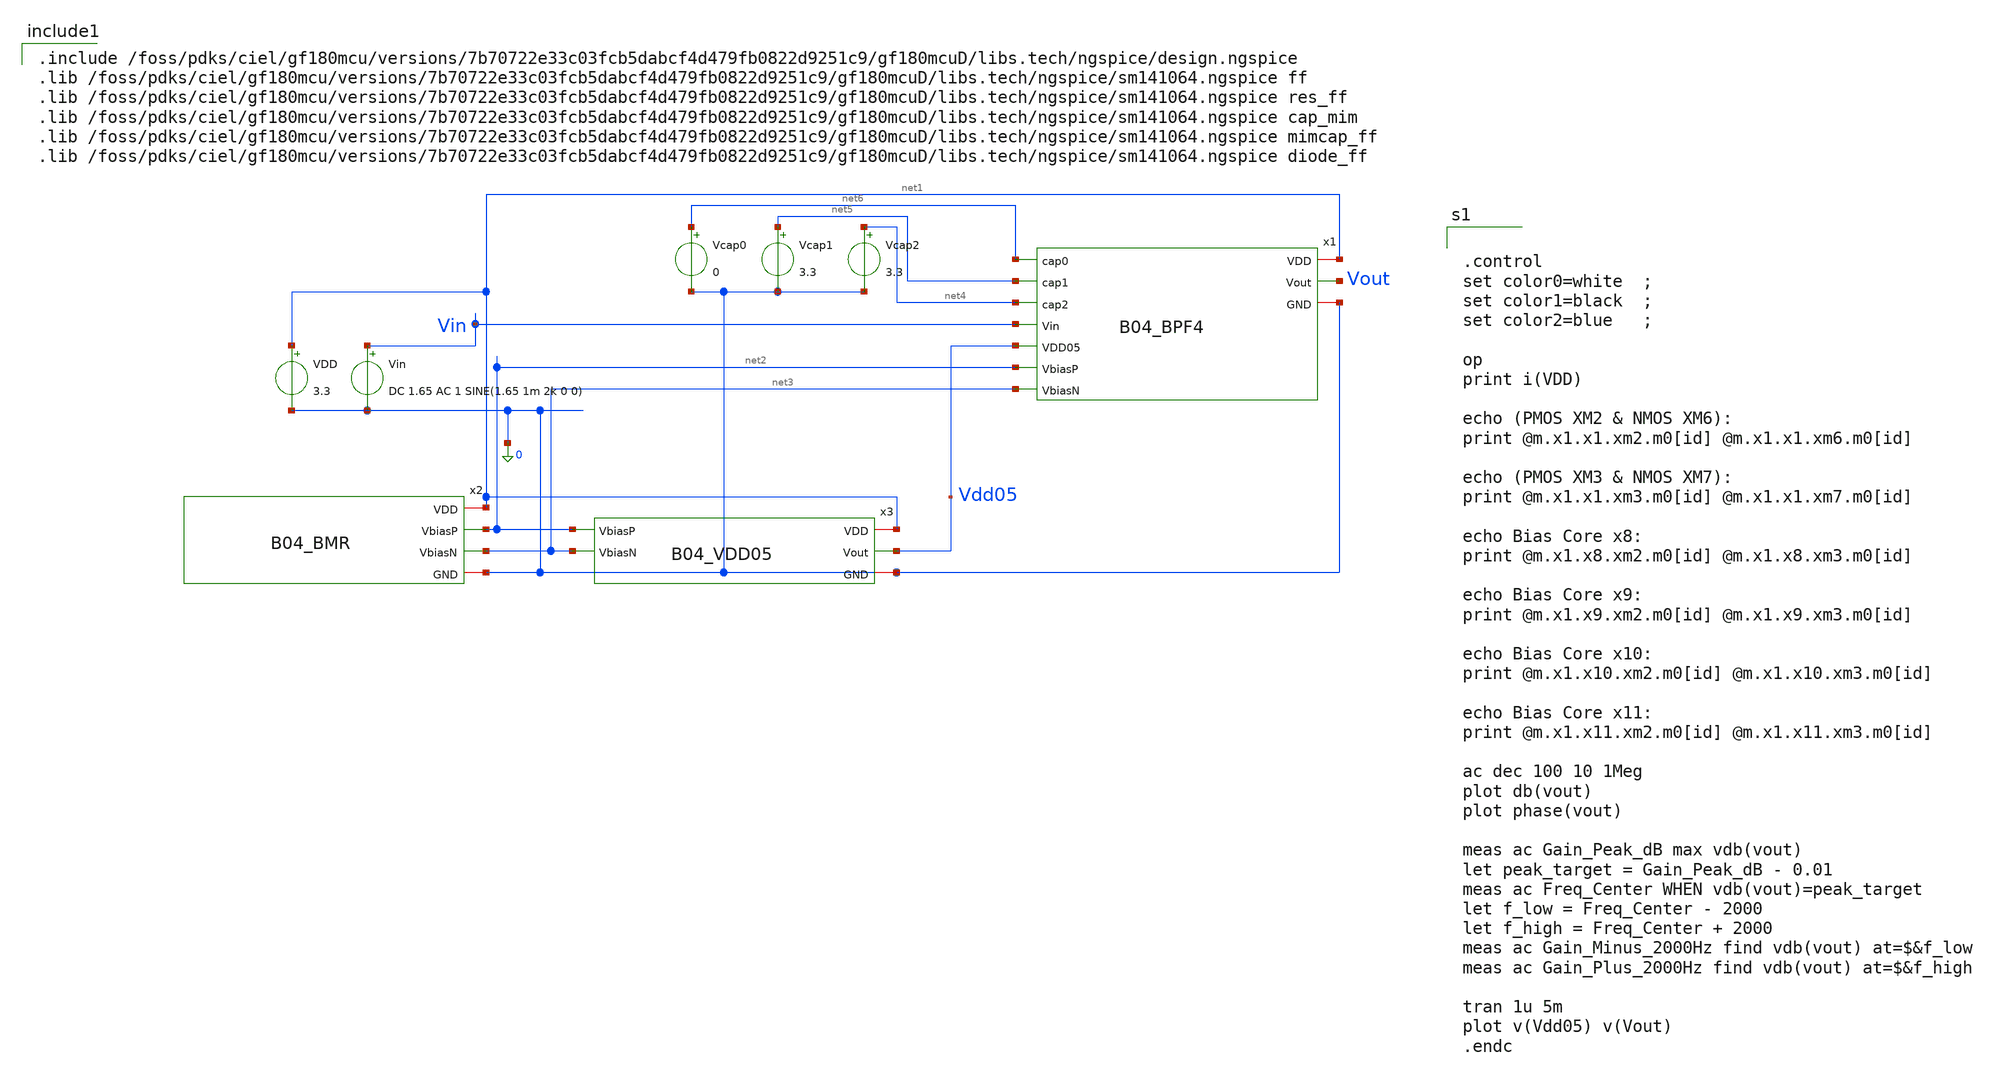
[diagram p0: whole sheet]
** sch_path: analog/B04_tb_BPF_4_order.sch
**.subckt B04_tb_BPF_4_order
Vin Vin 0 DC 1.65 AC 1 SINE(1.65 1m 2k 0 0)
VDD net1 0 3.3
x1 net6 net5 net4 net1 Vin Vout Vdd05 net2 net3 0 B04_BPF4
x2 net1 net2 net3 0 B04_BMR
x3 net1 Vdd05 0 net2 net3 B04_VDD05
Vcap0 net6 0 0
Vcap1 net5 0 3.3
Vcap2 net4 0 3.3
**** begin user architecture code

.include /foss/pdks/ciel/gf180mcu/versions/7b70722e33c03fcb5dabcf4d479fb0822d9251c9/gf180mcuD/libs.tech/ngspice/design.ngspice
.lib /foss/pdks/ciel/gf180mcu/versions/7b70722e33c03fcb5dabcf4d479fb0822d9251c9/gf180mcuD/libs.tech/ngspice/sm141064.ngspice ff
.lib /foss/pdks/ciel/gf180mcu/versions/7b70722e33c03fcb5dabcf4d479fb0822d9251c9/gf180mcuD/libs.tech/ngspice/sm141064.ngspice res_ff
.lib /foss/pdks/ciel/gf180mcu/versions/7b70722e33c03fcb5dabcf4d479fb0822d9251c9/gf180mcuD/libs.tech/ngspice/sm141064.ngspice cap_mim
.lib /foss/pdks/ciel/gf180mcu/versions/7b70722e33c03fcb5dabcf4d479fb0822d9251c9/gf180mcuD/libs.tech/ngspice/sm141064.ngspice mimcap_ff
.lib /foss/pdks/ciel/gf180mcu/versions/7b70722e33c03fcb5dabcf4d479fb0822d9251c9/gf180mcuD/libs.tech/ngspice/sm141064.ngspice diode_ff



.control
set color0=white  ;
set color1=black  ;
set color2=blue   ;

op
print i(VDD)

echo (PMOS XM2 & NMOS XM6):
print @m.x1.x1.xm2.m0[id] @m.x1.x1.xm6.m0[id]

echo (PMOS XM3 & NMOS XM7):
print @m.x1.x1.xm3.m0[id] @m.x1.x1.xm7.m0[id]

echo Bias Core x8:
print @m.x1.x8.xm2.m0[id] @m.x1.x8.xm3.m0[id]

echo Bias Core x9:
print @m.x1.x9.xm2.m0[id] @m.x1.x9.xm3.m0[id]

echo Bias Core x10:
print @m.x1.x10.xm2.m0[id] @m.x1.x10.xm3.m0[id]

echo Bias Core x11:
print @m.x1.x11.xm2.m0[id] @m.x1.x11.xm3.m0[id]

ac dec 100 10 1Meg
plot db(vout)
plot phase(vout)

meas ac Gain_Peak_dB max vdb(vout)
let peak_target = Gain_Peak_dB - 0.01
meas ac Freq_Center WHEN vdb(vout)=peak_target
let f_low = Freq_Center - 2000
let f_high = Freq_Center + 2000
meas ac Gain_Minus_2000Hz find vdb(vout) at=$&f_low
meas ac Gain_Plus_2000Hz find vdb(vout) at=$&f_high

tran 1u 5m
plot v(Vdd05) v(Vout)
.endc



**** end user architecture code
**.ends
.end
